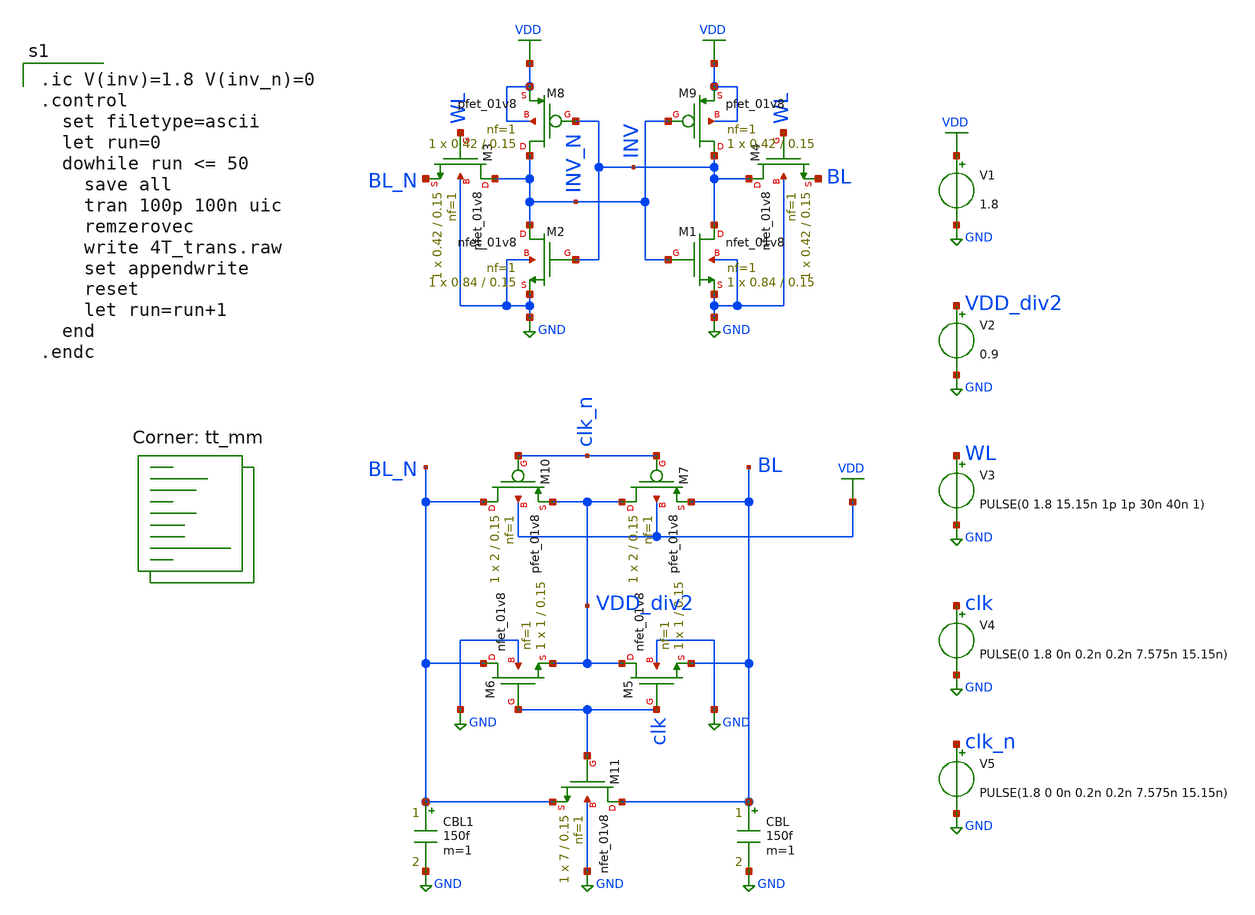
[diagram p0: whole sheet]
** sch_path: analog/schematics/4T_trans.sch
**.subckt 4T_trans
XM1 INV INV_N GND GND sky130_fd_pr__nfet_01v8 L=0.15 W=0.84 nf=1 ad='int((nf+1)/2) * W/nf * 0.29' as='int((nf+2)/2) * W/nf * 0.29'
+ pd='2*int((nf+1)/2) * (W/nf + 0.29)' ps='2*int((nf+2)/2) * (W/nf + 0.29)' nrd='0.29 / W' nrs='0.29 / W'
+ sa=0 sb=0 sd=0 mult=1 m=1
XM3 INV_N WL BL_N GND sky130_fd_pr__nfet_01v8 L=0.15 W=0.42 nf=1 ad='int((nf+1)/2) * W/nf * 0.29' as='int((nf+2)/2) * W/nf * 0.29'
+ pd='2*int((nf+1)/2) * (W/nf + 0.29)' ps='2*int((nf+2)/2) * (W/nf + 0.29)' nrd='0.29 / W' nrs='0.29 / W'
+ sa=0 sb=0 sd=0 mult=1 m=1
XM4 INV WL BL GND sky130_fd_pr__nfet_01v8 L=0.15 W=0.42 nf=1 ad='int((nf+1)/2) * W/nf * 0.29' as='int((nf+2)/2) * W/nf * 0.29'
+ pd='2*int((nf+1)/2) * (W/nf + 0.29)' ps='2*int((nf+2)/2) * (W/nf + 0.29)' nrd='0.29 / W' nrs='0.29 / W'
+ sa=0 sb=0 sd=0 mult=1 m=1
V1 VDD GND 1.8
V2 VDD_div2 GND 0.9
V3 WL GND PULSE(0 1.8 15.15n 1p 1p 30n 40n 1)
V4 clk GND PULSE(0 1.8 0n 0.2n 0.2n 7.575n 15.15n)
XM2 INV_N INV GND GND sky130_fd_pr__nfet_01v8 L=0.15 W=0.84 nf=1 ad='int((nf+1)/2) * W/nf * 0.29' as='int((nf+2)/2) * W/nf * 0.29'
+ pd='2*int((nf+1)/2) * (W/nf + 0.29)' ps='2*int((nf+2)/2) * (W/nf + 0.29)' nrd='0.29 / W' nrs='0.29 / W'
+ sa=0 sb=0 sd=0 mult=1 m=1
XM8 INV_N INV VDD VDD sky130_fd_pr__pfet_01v8 L=0.15 W=0.42 nf=1 ad='int((nf+1)/2) * W/nf * 0.29' as='int((nf+2)/2) * W/nf * 0.29'
+ pd='2*int((nf+1)/2) * (W/nf + 0.29)' ps='2*int((nf+2)/2) * (W/nf + 0.29)' nrd='0.29 / W' nrs='0.29 / W'
+ sa=0 sb=0 sd=0 mult=1 m=1
XM9 INV INV_N VDD VDD sky130_fd_pr__pfet_01v8 L=0.15 W=0.42 nf=1 ad='int((nf+1)/2) * W/nf * 0.29' as='int((nf+2)/2) * W/nf * 0.29'
+ pd='2*int((nf+1)/2) * (W/nf + 0.29)' ps='2*int((nf+2)/2) * (W/nf + 0.29)' nrd='0.29 / W' nrs='0.29 / W'
+ sa=0 sb=0 sd=0 mult=1 m=1
XM5 VDD_div2 clk BL GND sky130_fd_pr__nfet_01v8 L=0.15 W=1 nf=1 ad='int((nf+1)/2) * W/nf * 0.29' as='int((nf+2)/2) * W/nf * 0.29'
+ pd='2*int((nf+1)/2) * (W/nf + 0.29)' ps='2*int((nf+2)/2) * (W/nf + 0.29)' nrd='0.29 / W' nrs='0.29 / W'
+ sa=0 sb=0 sd=0 mult=1 m=1
XM6 BL_N clk VDD_div2 GND sky130_fd_pr__nfet_01v8 L=0.15 W=1 nf=1 ad='int((nf+1)/2) * W/nf * 0.29' as='int((nf+2)/2) * W/nf * 0.29'
+ pd='2*int((nf+1)/2) * (W/nf + 0.29)' ps='2*int((nf+2)/2) * (W/nf + 0.29)' nrd='0.29 / W' nrs='0.29 / W'
+ sa=0 sb=0 sd=0 mult=1 m=1
XM7 VDD_div2 clk_n BL VDD sky130_fd_pr__pfet_01v8 L=0.15 W=2 nf=1 ad='int((nf+1)/2) * W/nf * 0.29' as='int((nf+2)/2) * W/nf * 0.29'
+ pd='2*int((nf+1)/2) * (W/nf + 0.29)' ps='2*int((nf+2)/2) * (W/nf + 0.29)' nrd='0.29 / W' nrs='0.29 / W'
+ sa=0 sb=0 sd=0 mult=1 m=1
XM10 BL_N clk_n VDD_div2 VDD sky130_fd_pr__pfet_01v8 L=0.15 W=2 nf=1 ad='int((nf+1)/2) * W/nf * 0.29'
+ as='int((nf+2)/2) * W/nf * 0.29' pd='2*int((nf+1)/2) * (W/nf + 0.29)' ps='2*int((nf+2)/2) * (W/nf + 0.29)'
+ nrd='0.29 / W' nrs='0.29 / W' sa=0 sb=0 sd=0 mult=1 m=1
XM11 BL clk BL_N GND sky130_fd_pr__nfet_01v8 L=0.15 W=7 nf=1 ad='int((nf+1)/2) * W/nf * 0.29' as='int((nf+2)/2) * W/nf * 0.29'
+ pd='2*int((nf+1)/2) * (W/nf + 0.29)' ps='2*int((nf+2)/2) * (W/nf + 0.29)' nrd='0.29 / W' nrs='0.29 / W'
+ sa=0 sb=0 sd=0 mult=1 m=1
CBL BL GND 150f m=1
CBL1 BL_N GND 150f m=1
V5 clk_n GND PULSE(1.8 0 0n 0.2n 0.2n 7.575n 15.15n)
**** begin user architecture code

.ic V(inv)=1.8 V(inv_n)=0
.control
  set filetype=ascii
  let run=0
  dowhile run <= 50
    save all
    tran 100p 100n uic
    remzerovec
    write 4T_trans.raw
    set appendwrite
    reset
    let run=run+1
  end
.endc

.lib $::SKYWATER_MODELS/sky130.lib.spice tt_mm
**** end user architecture code
**.ends
.GLOBAL VDD
.GLOBAL GND
.end
